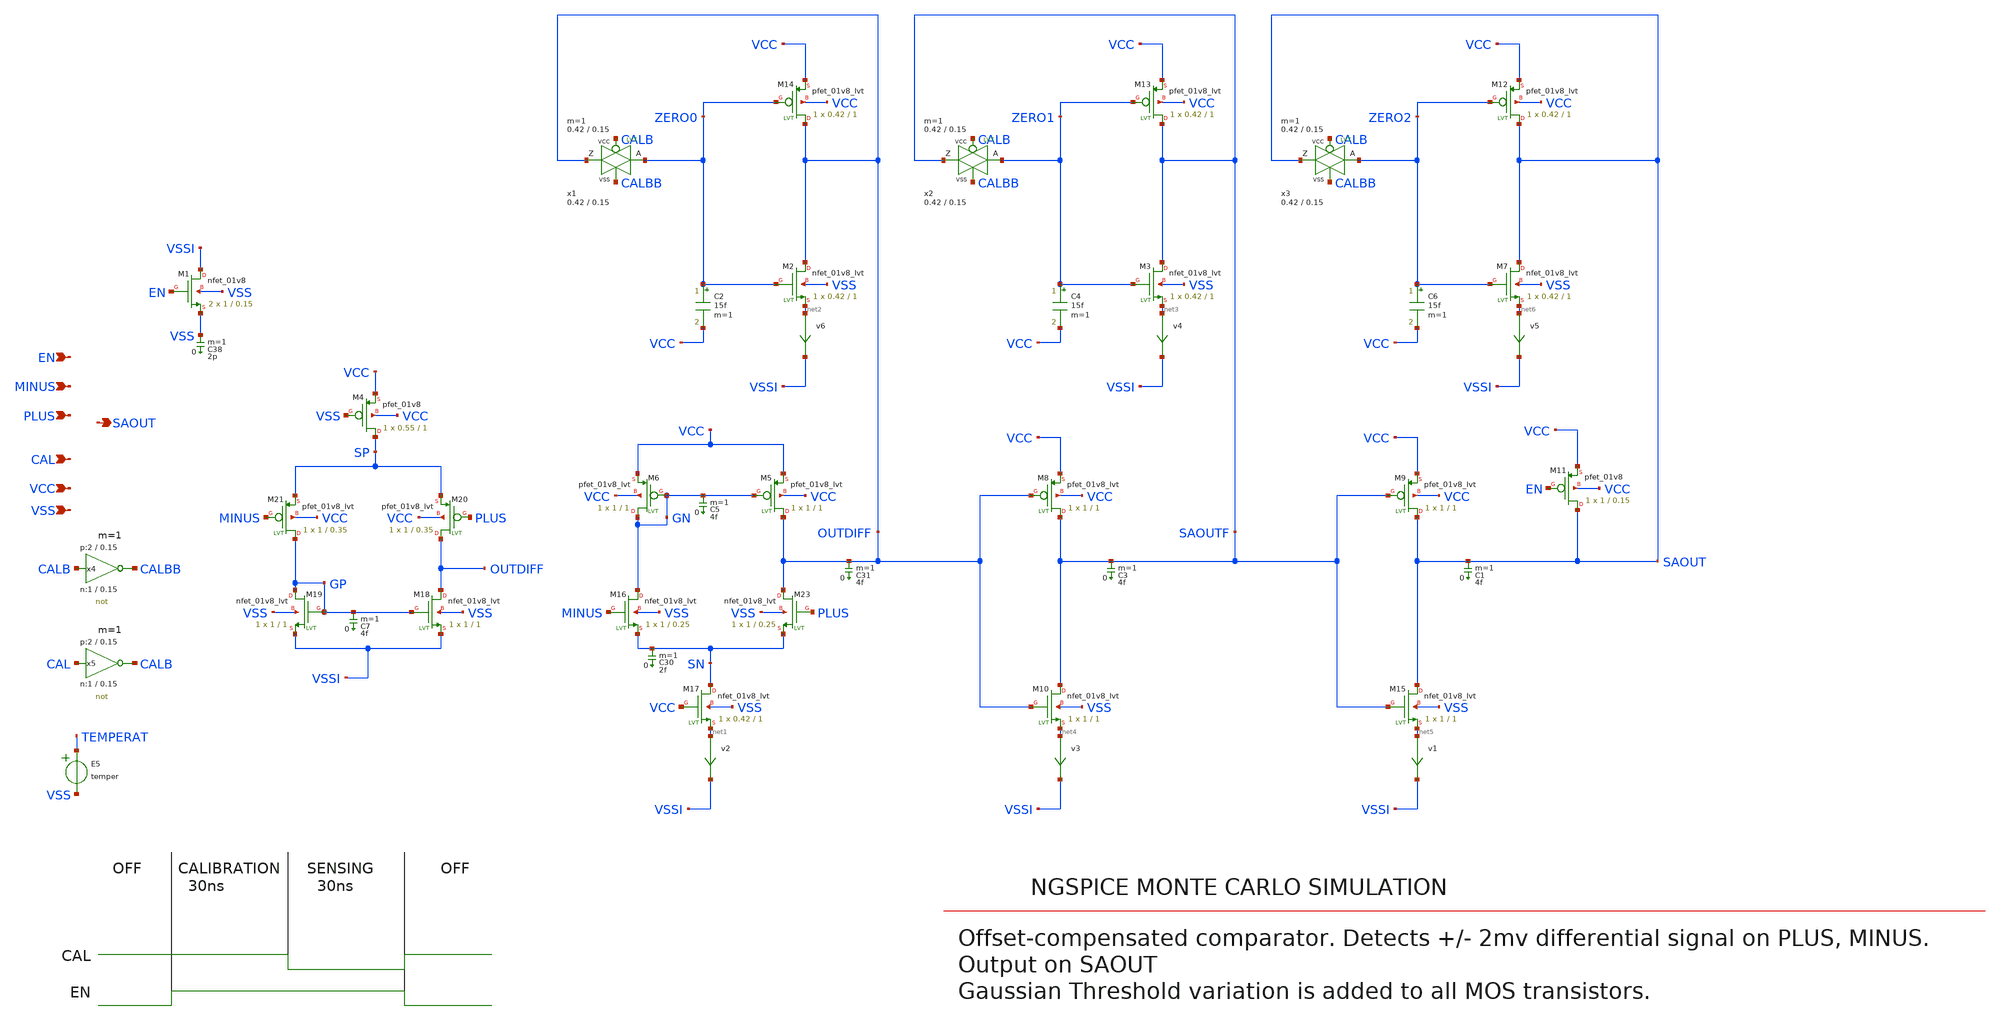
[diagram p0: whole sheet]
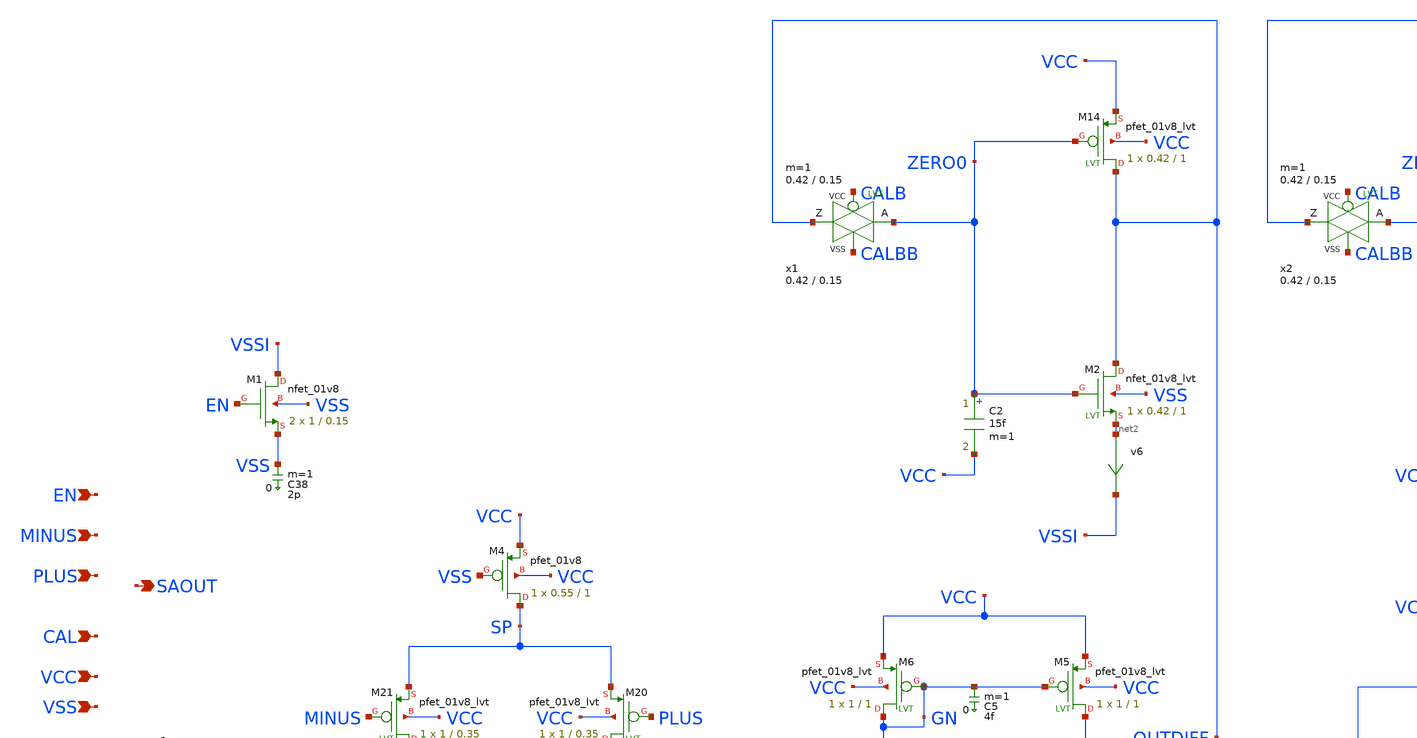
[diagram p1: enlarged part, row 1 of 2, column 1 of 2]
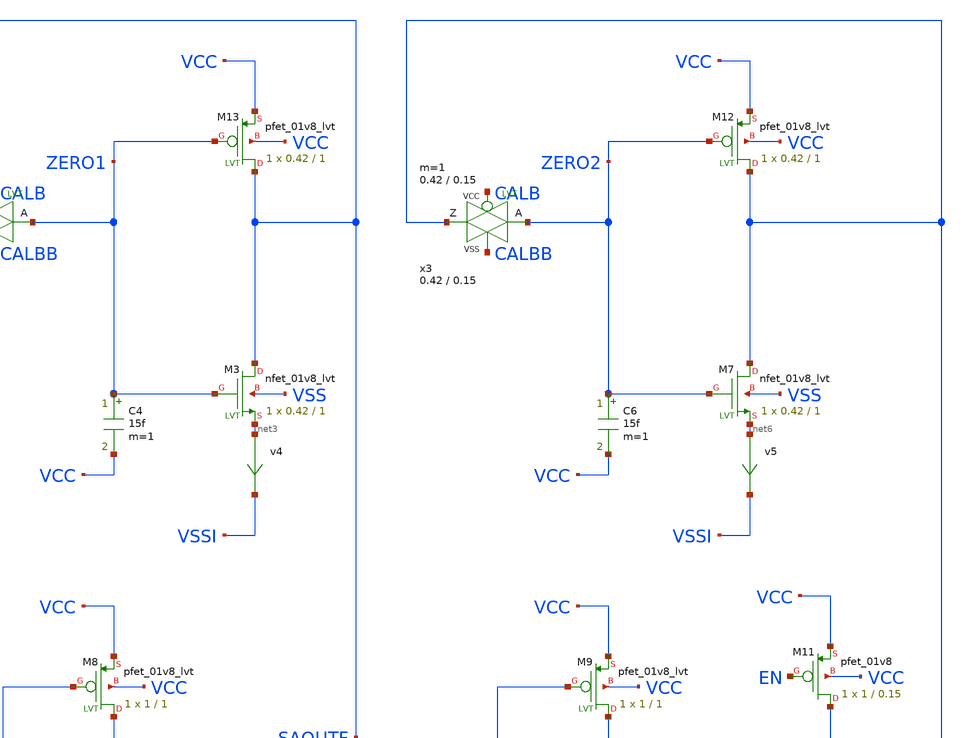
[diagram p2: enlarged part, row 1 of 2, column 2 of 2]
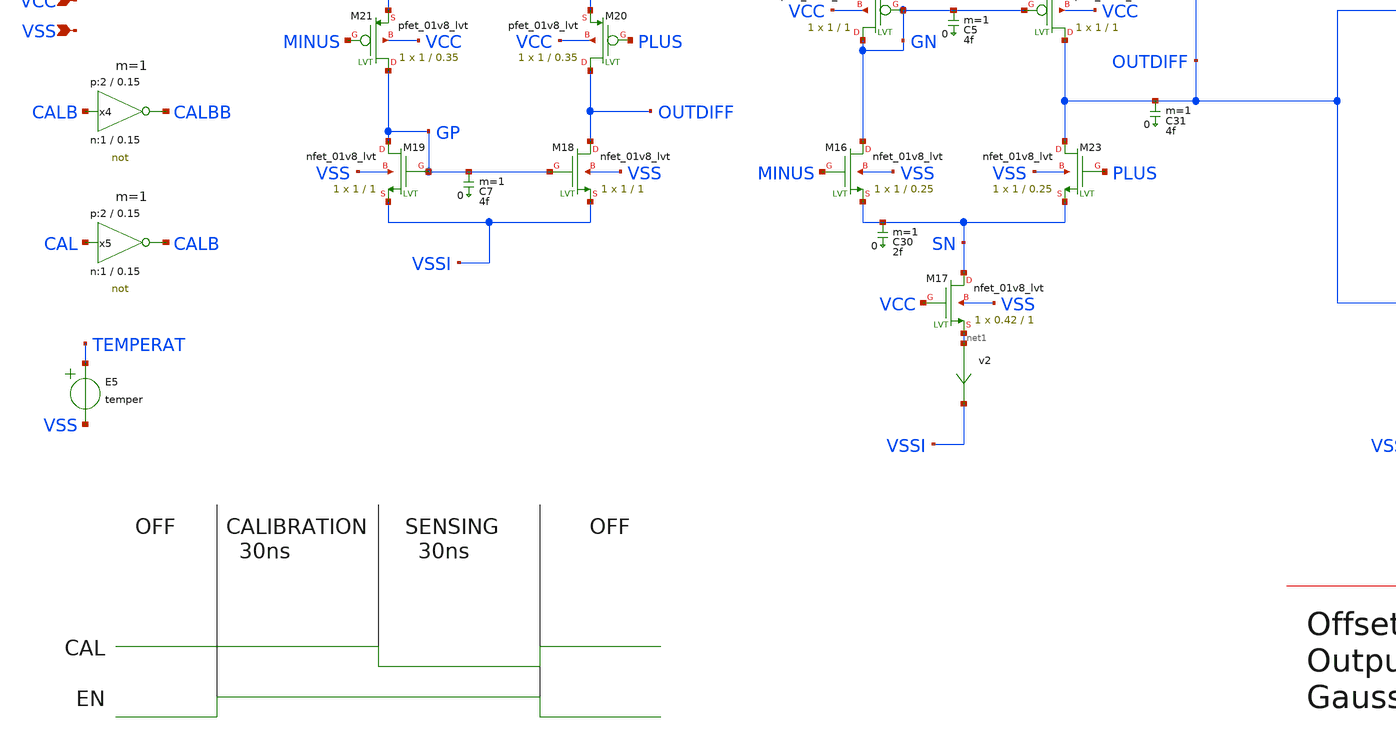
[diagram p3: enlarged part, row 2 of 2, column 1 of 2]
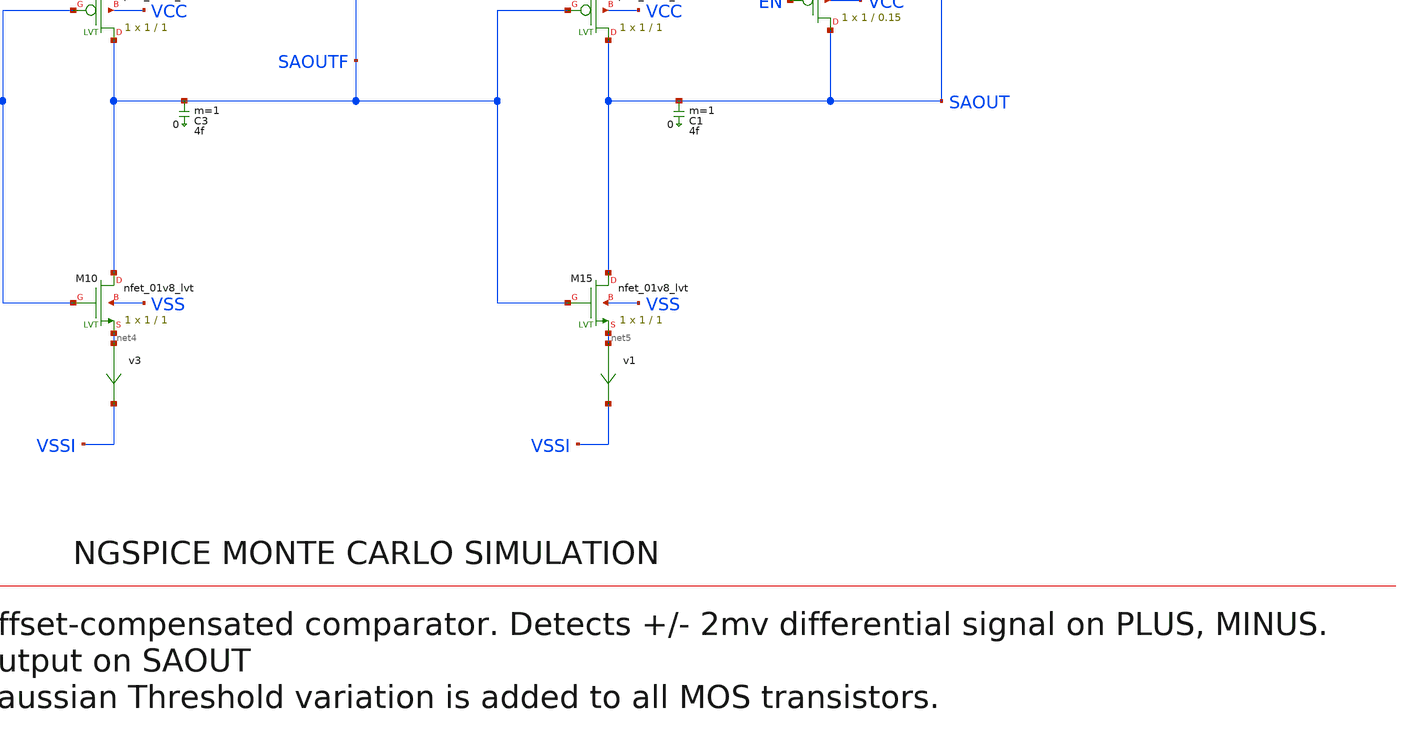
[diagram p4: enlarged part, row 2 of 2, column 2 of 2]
** sch_path: xyce/sky130A-xyce/libs.tech/xschem/sky130_tests/test_comparator.sch
* Copyright 2020 Stefan Frederik Schippers
* Licensed under the Apache License, Version 2.0 (the "License");
* you may not use this file except in compliance with the License.
* You may obtain a copy of the License at
* https://www.apache.org/licenses/LICENSE-2.0
* Unless required by applicable law or agreed to in writing, software
* distributed under the License is distributed on an "AS IS" BASIS,
* WITHOUT WARRANTIES OR CONDITIONS OF ANY KIND, either express or implied.
* See the License for the specific language governing permissions and
* limitations under the License.
**.subckt test_comparator CAL PLUS MINUS EN VSS VCC SAOUT
*.ipin CAL
*.ipin PLUS
*.ipin MINUS
*.ipin EN
*.ipin VSS
*.ipin VCC
*.opin SAOUT
E5 TEMPERAT VSS VOL=' temper '
C38 VSS 0 2p m=1
C3 SAOUTF 0 4f m=1
C5 GN 0 4f m=1
C30 SN 0 2f m=1
C31 OUTDIFF 0 4f m=1
v2 net1 VSSI 0
.save i(v2)
v3 net4 VSSI 0
.save i(v3)
v4 net3 VSSI 0
.save i(v4)
v6 net2 VSSI 0
.save i(v6)
C1 SAOUT 0 4f m=1
v1 net5 VSSI 0
.save i(v1)
v5 net6 VSSI 0
.save i(v5)
C7 GP 0 4f m=1
x4 CALBB CALB VCC VSS not W_N=1 L_N=0.15 W_P=2 L_P=0.15 m=1
x5 CALB CAL VCC VSS not W_N=1 L_N=0.15 W_P=2 L_P=0.15 m=1
XM4 SP VSS VCC VCC sky130_fd_pr__pfet_01v8 L=1 W=0.55 nf=1 ad='W * 0.29' as='W * 0.29' pd='W + 2 * 0.29'
+ ps='W + 2 * 0.29' nrd=0 nrs=0 sa=0 sb=0 sd=0 mult=1 m=1
XM5 OUTDIFF GN VCC VCC sky130_fd_pr__pfet_01v8_lvt L=1 W=1 nf=1 ad='W * 0.29' as='W * 0.29' pd='2*(W + 0.29)'
+ ps='2*(W + 0.29)' nrd=0 nrs=0 sa=0 sb=0 sd=0 mult=1 m=1
XM6 GN GN VCC VCC sky130_fd_pr__pfet_01v8_lvt L=1 W=1 nf=1 ad='W * 0.29' as='W * 0.29' pd='2*(W + 0.29)'
+ ps='2*(W + 0.29)' nrd=0 nrs=0 sa=0 sb=0 sd=0 mult=1 m=1
XM8 SAOUTF OUTDIFF VCC VCC sky130_fd_pr__pfet_01v8_lvt L=1 W=1 nf=1 ad='W * 0.29' as='W * 0.29' pd='2*(W + 0.29)'
+ ps='2*(W + 0.29)' nrd=0 nrs=0 sa=0 sb=0 sd=0 mult=1 m=1
XM9 SAOUT SAOUTF VCC VCC sky130_fd_pr__pfet_01v8_lvt L=1 W=1 nf=1 ad='W * 0.29' as='W * 0.29' pd='2*(W + 0.29)'
+ ps='2*(W + 0.29)' nrd=0 nrs=0 sa=0 sb=0 sd=0 mult=1 m=1
XM11 SAOUT EN VCC VCC sky130_fd_pr__pfet_01v8 L=0.15 W=1 nf=1 ad='W * 0.29' as='W * 0.29' pd='W + 2 * 0.29'
+ ps='W + 2 * 0.29' nrd=0 nrs=0 sa=0 sb=0 sd=0 mult=1 m=1
XM12 SAOUT ZERO2 VCC VCC sky130_fd_pr__pfet_01v8_lvt L=1 W=0.42 nf=1 ad='W * 0.29' as='W * 0.29' pd='2*(W + 0.29)'
+ ps='2*(W + 0.29)' nrd=0 nrs=0 sa=0 sb=0 sd=0 mult=1 m=1
XM13 SAOUTF ZERO1 VCC VCC sky130_fd_pr__pfet_01v8_lvt L=1 W=0.42 nf=1 ad='W * 0.29' as='W * 0.29' pd='2*(W + 0.29)'
+ ps='2*(W + 0.29)' nrd=0 nrs=0 sa=0 sb=0 sd=0 mult=1 m=1
XM14 OUTDIFF ZERO0 VCC VCC sky130_fd_pr__pfet_01v8_lvt L=1 W=0.42 nf=1 ad='W * 0.29' as='W * 0.29' pd='2*(W + 0.29)'
+ ps='2*(W + 0.29)' nrd=0 nrs=0 sa=0 sb=0 sd=0 mult=1 m=1
XM1 VSSI EN VSS VSS sky130_fd_pr__nfet_01v8 L=0.15 W=1 nf=1 ad='W * 0.29' as='W * 0.29' pd='W + 2 * 0.29'
+ ps='W + 2 * 0.29' nrd=0 nrs=0 sa=0 sb=0 sd=0 mult=2 m=2
XM2 OUTDIFF ZERO0 net2 VSS sky130_fd_pr__nfet_01v8_lvt L=1 W=0.42 nf=1 ad='W * 0.29' as='W * 0.29' pd='2*(W + 0.29)'
+ ps='2*(W + 0.29)' nrd=0 nrs=0 sa=0 sb=0 sd=0 mult=1 m=1
XM3 SAOUTF ZERO1 net3 VSS sky130_fd_pr__nfet_01v8_lvt L=1 W=0.42 nf=1 ad='W * 0.29' as='W * 0.29' pd='2*(W + 0.29)'
+ ps='2*(W + 0.29)' nrd=0 nrs=0 sa=0 sb=0 sd=0 mult=1 m=1
XM7 SAOUT ZERO2 net6 VSS sky130_fd_pr__nfet_01v8_lvt L=1 W=0.42 nf=1 ad='W * 0.29' as='W * 0.29' pd='2*(W + 0.29)'
+ ps='2*(W + 0.29)' nrd=0 nrs=0 sa=0 sb=0 sd=0 mult=1 m=1
XM15 SAOUT SAOUTF net5 VSS sky130_fd_pr__nfet_01v8_lvt L=1 W=1 nf=1 ad='W * 0.29' as='W * 0.29' pd='2*(W + 0.29)'
+ ps='2*(W + 0.29)' nrd=0 nrs=0 sa=0 sb=0 sd=0 mult=1 m=1
XM10 SAOUTF OUTDIFF net4 VSS sky130_fd_pr__nfet_01v8_lvt L=1 W=1 nf=1 ad='W * 0.29' as='W * 0.29' pd='2*(W + 0.29)'
+ ps='2*(W + 0.29)' nrd=0 nrs=0 sa=0 sb=0 sd=0 mult=1 m=1
XM17 SN VCC net1 VSS sky130_fd_pr__nfet_01v8_lvt L=1 W=0.42 nf=1 ad='W * 0.29' as='W * 0.29' pd='2*(W + 0.29)'
+ ps='2*(W + 0.29)' nrd=0 nrs=0 sa=0 sb=0 sd=0 mult=1 m=1
XM18 OUTDIFF GP VSSI VSS sky130_fd_pr__nfet_01v8_lvt L=1 W=1 nf=1 ad='W * 0.29' as='W * 0.29' pd='2*(W + 0.29)'
+ ps='2*(W + 0.29)' nrd=0 nrs=0 sa=0 sb=0 sd=0 mult=1 m=1
XM19 GP GP VSSI VSS sky130_fd_pr__nfet_01v8_lvt L=1 W=1 nf=1 ad='W * 0.29' as='W * 0.29' pd='2*(W + 0.29)'
+ ps='2*(W + 0.29)' nrd=0 nrs=0 sa=0 sb=0 sd=0 mult=1 m=1
XM20 OUTDIFF PLUS SP VCC sky130_fd_pr__pfet_01v8_lvt L=0.35 W=1 nf=1 ad='W * 0.29' as='W * 0.29' pd='2*(W + 0.29)'
+ ps='2*(W + 0.29)' nrd=0 nrs=0 sa=0 sb=0 sd=0 mult=1 m=1
XM21 GP MINUS SP VCC sky130_fd_pr__pfet_01v8_lvt L=0.35 W=1 nf=1 ad='W * 0.29' as='W * 0.29' pd='2*(W + 0.29)'
+ ps='2*(W + 0.29)' nrd=0 nrs=0 sa=0 sb=0 sd=0 mult=1 m=1
XM23 OUTDIFF PLUS SN VSS sky130_fd_pr__nfet_01v8_lvt L=0.25 W=1 nf=1 ad='W * 0.29' as='W * 0.29' pd='2*(W + 0.29)'
+ ps='2*(W + 0.29)' nrd=0 nrs=0 sa=0 sb=0 sd=0 mult=1 m=1
XM16 GN MINUS SN VSS sky130_fd_pr__nfet_01v8_lvt L=0.25 W=1 nf=1 ad='W * 0.29' as='W * 0.29' pd='2*(W + 0.29)'
+ ps='2*(W + 0.29)' nrd=0 nrs=0 sa=0 sb=0 sd=0 mult=1 m=1
x1 OUTDIFF ZERO0 CALB CALBB VCC VSS passgate_nlvt W_N=0.42 L_N=0.15 W_P=0.42 L_P=0.15 m=1
x2 SAOUTF ZERO1 CALB CALBB VCC VSS passgate_nlvt W_N=0.42 L_N=0.15 W_P=0.42 L_P=0.15 m=1
x3 SAOUT ZERO2 CALB CALBB VCC VSS passgate_nlvt W_N=0.42 L_N=0.15 W_P=0.42 L_P=0.15 m=1
C2 ZERO0 VCC 15f m=1
C4 ZERO1 VCC 15f m=1
C6 ZERO2 VCC 15f m=1
**** begin user architecture code

.include $::SKYWATER_MODELS/cells/nfet_01v8/sky130_fd_pr__nfet_01v8__tt.corner.spice
.include $::SKYWATER_MODELS/cells/nfet_01v8_lvt/sky130_fd_pr__nfet_01v8_lvt__tt.corner.spice
.include $::SKYWATER_MODELS/cells/pfet_01v8/sky130_fd_pr__pfet_01v8__tt.corner.spice
.include $::SKYWATER_MODELS/cells/nfet_03v3_nvt/sky130_fd_pr__nfet_03v3_nvt__tt.corner.spice
.include $::SKYWATER_MODELS/cells/nfet_05v0_nvt/sky130_fd_pr__nfet_05v0_nvt__tt.corner.spice
.include $::SKYWATER_MODELS/cells/esd_nfet_01v8/sky130_fd_pr__esd_nfet_01v8__tt.corner.spice
.include $::SKYWATER_MODELS/cells/pfet_01v8_lvt/sky130_fd_pr__pfet_01v8_lvt__tt.corner.spice
.include $::SKYWATER_MODELS/cells/pfet_01v8_hvt/sky130_fd_pr__pfet_01v8_hvt__tt.corner.spice
.include $::SKYWATER_MODELS/cells/esd_pfet_g5v0d10v5/sky130_fd_pr__esd_pfet_g5v0d10v5__tt.corner.spice
.include $::SKYWATER_MODELS/cells/pfet_g5v0d10v5/sky130_fd_pr__pfet_g5v0d10v5__tt.corner.spice
.include $::SKYWATER_MODELS/cells/pfet_g5v0d16v0/sky130_fd_pr__pfet_g5v0d16v0__tt.corner.spice
.include $::SKYWATER_MODELS/cells/nfet_g5v0d10v5/sky130_fd_pr__nfet_g5v0d10v5__tt.corner.spice
.include $::SKYWATER_MODELS/cells/nfet_g5v0d16v0/sky130_fd_pr__nfet_g5v0d16v0__tt_discrete.corner.spice
.include $::SKYWATER_MODELS/cells/esd_nfet_g5v0d10v5/sky130_fd_pr__esd_nfet_g5v0d10v5__tt.corner.spice
.include $::SKYWATER_MODELS/models/corners/tt/nonfet.spice
* Mismatch parameters
.include $::SKYWATER_MODELS/cells/nfet_01v8/sky130_fd_pr__nfet_01v8__mismatch.corner.spice
.include $::SKYWATER_MODELS/cells/pfet_01v8/sky130_fd_pr__pfet_01v8__mismatch.corner.spice
.include $::SKYWATER_MODELS/cells/nfet_01v8_lvt/sky130_fd_pr__nfet_01v8_lvt__mismatch.corner.spice
.include $::SKYWATER_MODELS/cells/pfet_01v8_lvt/sky130_fd_pr__pfet_01v8_lvt__mismatch.corner.spice
.include $::SKYWATER_MODELS/cells/pfet_01v8_hvt/sky130_fd_pr__pfet_01v8_hvt__mismatch.corner.spice
.include $::SKYWATER_MODELS/cells/nfet_g5v0d10v5/sky130_fd_pr__nfet_g5v0d10v5__mismatch.corner.spice
.include $::SKYWATER_MODELS/cells/pfet_g5v0d10v5/sky130_fd_pr__pfet_g5v0d10v5__mismatch.corner.spice
.include $::SKYWATER_MODELS/cells/nfet_05v0_nvt/sky130_fd_pr__nfet_05v0_nvt__mismatch.corner.spice
.include $::SKYWATER_MODELS/cells/nfet_03v3_nvt/sky130_fd_pr__nfet_03v3_nvt__mismatch.corner.spice
* Resistor$::SKYWATER_MODELS/Capacitor
.include $::SKYWATER_MODELS/models/r+c/res_typical__cap_typical.spice
.include $::SKYWATER_MODELS/models/r+c/res_typical__cap_typical__lin.spice
* Special cells
.include $::SKYWATER_MODELS/models/corners/tt/specialized_cells.spice
* All models
.include $::SKYWATER_MODELS/models/all.spice
* Corner
.include $::SKYWATER_MODELS/models/corners/tt/rf.spice

**** end user architecture code
**.ends

* expanding   symbol:  sky130_tests/not.sym # of pins=2
** sym_path: xyce/sky130A-xyce/libs.tech/xschem/sky130_tests/not.sym
** sch_path: xyce/sky130A-xyce/libs.tech/xschem/sky130_tests/not.sch
.subckt not y a VCCPIN VSSPIN     W_N=1 L_N=0.15 W_P=2 L_P=0.15
*.opin y
*.ipin a
XM1 y a VSSPIN VSSPIN sky130_fd_pr__nfet_01v8 L=L_N W=W_N nf=1 ad='int((nf+1)/2) * W/nf * 0.29' as='int((nf+2)/2) * W/nf * 0.29'
+ pd='2*int((nf+1)/2) * (W/nf + 0.29)' ps='2*int((nf+2)/2) * (W/nf + 0.29)' nrd='0.29 / W' nrs='0.29 / W'
+ sa=0 sb=0 sd=0 mult=1 m=1
XM2 y a VCCPIN VCCPIN sky130_fd_pr__pfet_01v8 L=L_P W=W_P nf=1 ad='int((nf+1)/2) * W/nf * 0.29' as='int((nf+2)/2) * W/nf * 0.29'
+ pd='2*int((nf+1)/2) * (W/nf + 0.29)' ps='2*int((nf+2)/2) * (W/nf + 0.29)' nrd='0.29 / W' nrs='0.29 / W'
+ sa=0 sb=0 sd=0 mult=1 m=1
.ends


* expanding   symbol:  sky130_tests/passgate_nlvt.sym # of pins=4
** sym_path: xyce/sky130A-xyce/libs.tech/xschem/sky130_tests/passgate_nlvt.sym
** sch_path: xyce/sky130A-xyce/libs.tech/xschem/sky130_tests/passgate_nlvt.sch
.subckt passgate_nlvt Z A GP GN VCCBPIN VSSBPIN  W_N=1 L_N=0.35 W_P=1 L_P=0.35
*.iopin A
*.iopin Z
*.ipin GP
*.ipin GN
XM1 Z GN A VSSBPIN sky130_fd_pr__nfet_01v8_lvt L=L_N W=W_N nf=1 ad='int((nf+1)/2) * W/nf * 0.29' as='int((nf+2)/2) * W/nf * 0.29'
+ pd='2*int((nf+1)/2) * (W/nf + 0.29)' ps='2*int((nf+2)/2) * (W/nf + 0.29)' nrd='0.29 / W' nrs='0.29 / W'
+ sa=0 sb=0 sd=0 mult=1 m=1
XM2 Z GP A VCCBPIN sky130_fd_pr__pfet_01v8_lvt L=L_P W=W_P nf=1 ad='int((nf+1)/2) * W/nf * 0.29' as='int((nf+2)/2) * W/nf * 0.29'
+ pd='2*int((nf+1)/2) * (W/nf + 0.29)' ps='2*int((nf+2)/2) * (W/nf + 0.29)' nrd='0.29 / W' nrs='0.29 / W'
+ sa=0 sb=0 sd=0 mult=1 m=1
.ends

**** begin user architecture code

* .option SCALE=1e-6
.option method=gear seed=12

* this experimental option enables mos model bin
* selection based on W/NF instead of W
.option wnflag=1

* .param VCC=1.8
.param VCCGAUSS=agauss(1.8, 0.05, 1)
.param VCC=VCCGAUSS
.param VDL='VCC/2+0.2'
.param ABSVAR=0.02
.temp 25

** to generate following file:
** copy .../xschem_sky130/sky130_tests/stimuli.test_comparator to simulation directory
** then do 'Simulation->Utile Stimuli Editor (GUI)' and press 'Translate'
.include "stimuli_test_comparator.cir"

** variation marameters:
.param sky130_fd_pr__nfet_01v8_lvt__vth0_slope_spectre='agauss(0, ABSVAR, 3)/sky130_fd_pr__nfet_01v8_lvt__vth0_slope'
.param sky130_fd_pr__pfet_01v8_lvt__vth0_slope_spectre='agauss(0, ABSVAR, 3)/sky130_fd_pr__pfet_01v8_lvt__vth0_slope'

* .tran 0.1n 900n uic

.control
  let run=1
  dowhile run <= 20
    if run > 1
      reset
      set appendwrite
    end
    save all
    * save saout cal i(vvcc) en plus minus
    tran 0.1n 300n uic
    write test_comparator.raw
    let run = run + 1
  end
.endc


**** end user architecture code
.end
